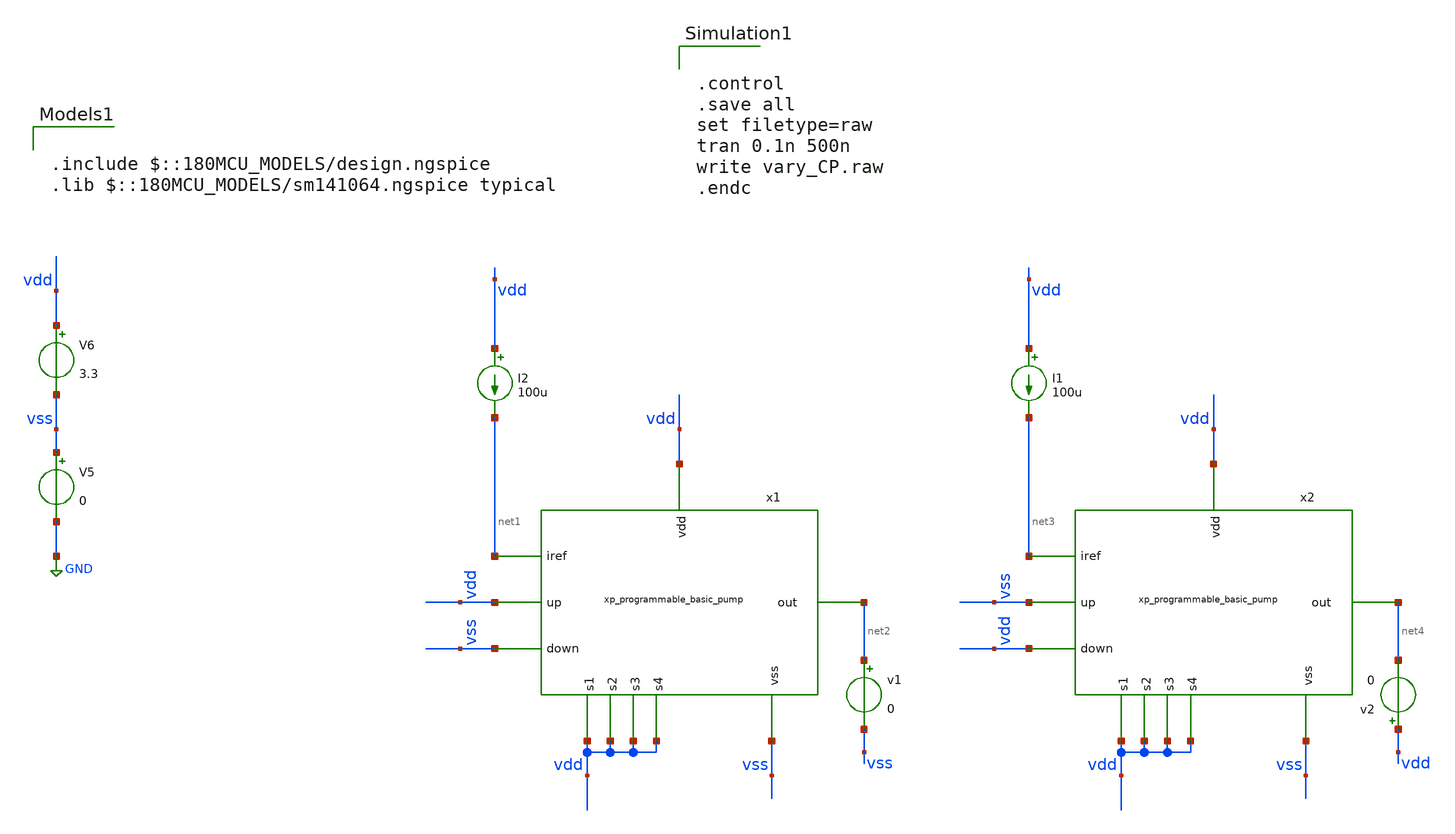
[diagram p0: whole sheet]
** sch_path: designs/libs/xp_tb_analog/tb_PFD_CP.sch
**.subckt tb_PFD_CP
V5 vss GND 0
V6 vdd vss 3.3
I2 vdd net1 100u
x1 vdd net2 vss vdd vdd vdd vdd vss vdd net1 xp_programmable_basic_pump
v1 net2 vss 0
I1 vdd net3 100u
x2 vdd net4 vss vdd vdd vdd vdd vdd vss net3 xp_programmable_basic_pump
v2 vdd net4 0
**** begin user architecture code

.include $::180MCU_MODELS/design.ngspice
.lib $::180MCU_MODELS/sm141064.ngspice typical



.control
.save all
set filetype=raw
tran 0.1n 500n
write vary_CP.raw
.endc


**** end user architecture code
**.ends
.GLOBAL GND
.end
